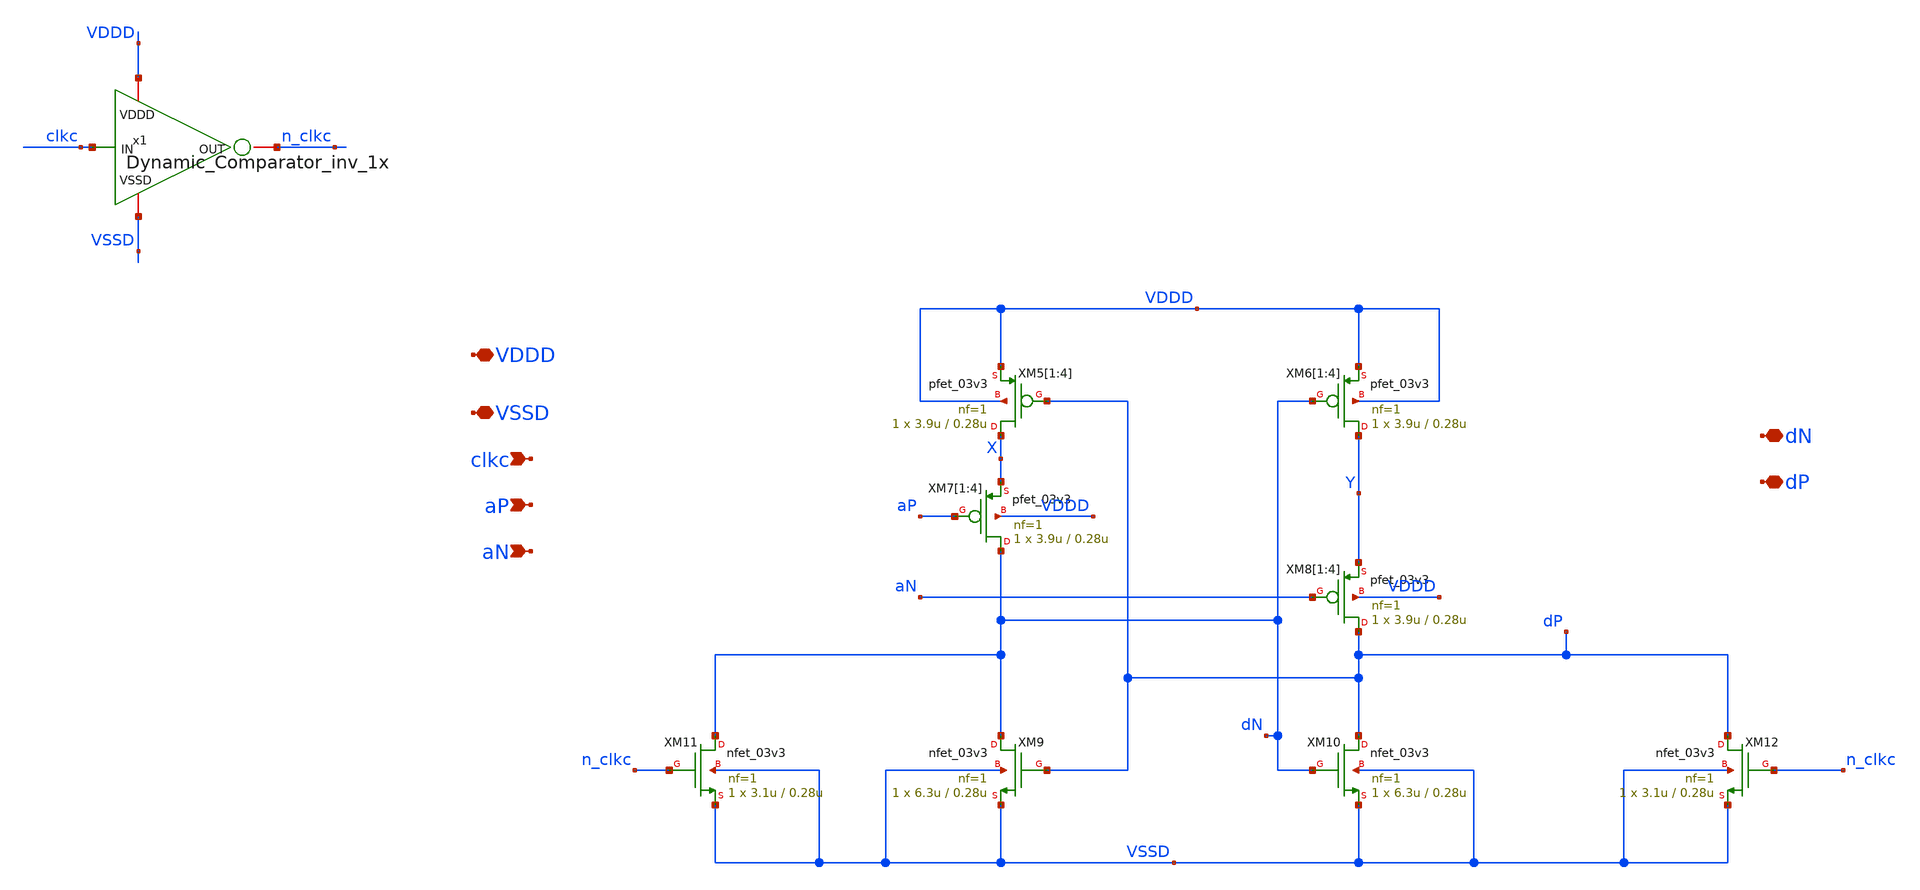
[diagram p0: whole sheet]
** sch_path: SAR_ADC/Dynamic_Comparator/xschem/Dynamic_Comparator_latch.sch
**.subckt Dynamic_Comparator_latch VDDD VSSD clkc aP aN dN dP
*.iopin VDDD
*.iopin VSSD
*.ipin clkc
*.ipin aP
*.ipin aN
*.iopin dN
*.iopin dP
XM5[1] X dP VDDD VDDD pfet_03v3 L=0.28u W=3.9u nf=1 ad='int((nf+1)/2) * W/nf * 0.18u' as='int((nf+2)/2) * W/nf * 0.18u'
+ pd='2*int((nf+1)/2) * (W/nf + 0.18u)' ps='2*int((nf+2)/2) * (W/nf + 0.18u)' nrd='0.18u / W' nrs='0.18u / W'
+ sa=0 sb=0 sd=0 m=1
XM5[2] X dP VDDD VDDD pfet_03v3 L=0.28u W=3.9u nf=1 ad='int((nf+1)/2) * W/nf * 0.18u' as='int((nf+2)/2) * W/nf * 0.18u'
+ pd='2*int((nf+1)/2) * (W/nf + 0.18u)' ps='2*int((nf+2)/2) * (W/nf + 0.18u)' nrd='0.18u / W' nrs='0.18u / W'
+ sa=0 sb=0 sd=0 m=1
XM5[3] X dP VDDD VDDD pfet_03v3 L=0.28u W=3.9u nf=1 ad='int((nf+1)/2) * W/nf * 0.18u' as='int((nf+2)/2) * W/nf * 0.18u'
+ pd='2*int((nf+1)/2) * (W/nf + 0.18u)' ps='2*int((nf+2)/2) * (W/nf + 0.18u)' nrd='0.18u / W' nrs='0.18u / W'
+ sa=0 sb=0 sd=0 m=1
XM5[4] X dP VDDD VDDD pfet_03v3 L=0.28u W=3.9u nf=1 ad='int((nf+1)/2) * W/nf * 0.18u' as='int((nf+2)/2) * W/nf * 0.18u'
+ pd='2*int((nf+1)/2) * (W/nf + 0.18u)' ps='2*int((nf+2)/2) * (W/nf + 0.18u)' nrd='0.18u / W' nrs='0.18u / W'
+ sa=0 sb=0 sd=0 m=1
XM6[1] Y dN VDDD VDDD pfet_03v3 L=0.28u W=3.9u nf=1 ad='int((nf+1)/2) * W/nf * 0.18u' as='int((nf+2)/2) * W/nf * 0.18u'
+ pd='2*int((nf+1)/2) * (W/nf + 0.18u)' ps='2*int((nf+2)/2) * (W/nf + 0.18u)' nrd='0.18u / W' nrs='0.18u / W'
+ sa=0 sb=0 sd=0 m=1
XM6[2] Y dN VDDD VDDD pfet_03v3 L=0.28u W=3.9u nf=1 ad='int((nf+1)/2) * W/nf * 0.18u' as='int((nf+2)/2) * W/nf * 0.18u'
+ pd='2*int((nf+1)/2) * (W/nf + 0.18u)' ps='2*int((nf+2)/2) * (W/nf + 0.18u)' nrd='0.18u / W' nrs='0.18u / W'
+ sa=0 sb=0 sd=0 m=1
XM6[3] Y dN VDDD VDDD pfet_03v3 L=0.28u W=3.9u nf=1 ad='int((nf+1)/2) * W/nf * 0.18u' as='int((nf+2)/2) * W/nf * 0.18u'
+ pd='2*int((nf+1)/2) * (W/nf + 0.18u)' ps='2*int((nf+2)/2) * (W/nf + 0.18u)' nrd='0.18u / W' nrs='0.18u / W'
+ sa=0 sb=0 sd=0 m=1
XM6[4] Y dN VDDD VDDD pfet_03v3 L=0.28u W=3.9u nf=1 ad='int((nf+1)/2) * W/nf * 0.18u' as='int((nf+2)/2) * W/nf * 0.18u'
+ pd='2*int((nf+1)/2) * (W/nf + 0.18u)' ps='2*int((nf+2)/2) * (W/nf + 0.18u)' nrd='0.18u / W' nrs='0.18u / W'
+ sa=0 sb=0 sd=0 m=1
XM7[1] dN aP X VDDD pfet_03v3 L=0.28u W=3.9u nf=1 ad='int((nf+1)/2) * W/nf * 0.18u' as='int((nf+2)/2) * W/nf * 0.18u'
+ pd='2*int((nf+1)/2) * (W/nf + 0.18u)' ps='2*int((nf+2)/2) * (W/nf + 0.18u)' nrd='0.18u / W' nrs='0.18u / W'
+ sa=0 sb=0 sd=0 m=1
XM7[2] dN aP X VDDD pfet_03v3 L=0.28u W=3.9u nf=1 ad='int((nf+1)/2) * W/nf * 0.18u' as='int((nf+2)/2) * W/nf * 0.18u'
+ pd='2*int((nf+1)/2) * (W/nf + 0.18u)' ps='2*int((nf+2)/2) * (W/nf + 0.18u)' nrd='0.18u / W' nrs='0.18u / W'
+ sa=0 sb=0 sd=0 m=1
XM7[3] dN aP X VDDD pfet_03v3 L=0.28u W=3.9u nf=1 ad='int((nf+1)/2) * W/nf * 0.18u' as='int((nf+2)/2) * W/nf * 0.18u'
+ pd='2*int((nf+1)/2) * (W/nf + 0.18u)' ps='2*int((nf+2)/2) * (W/nf + 0.18u)' nrd='0.18u / W' nrs='0.18u / W'
+ sa=0 sb=0 sd=0 m=1
XM7[4] dN aP X VDDD pfet_03v3 L=0.28u W=3.9u nf=1 ad='int((nf+1)/2) * W/nf * 0.18u' as='int((nf+2)/2) * W/nf * 0.18u'
+ pd='2*int((nf+1)/2) * (W/nf + 0.18u)' ps='2*int((nf+2)/2) * (W/nf + 0.18u)' nrd='0.18u / W' nrs='0.18u / W'
+ sa=0 sb=0 sd=0 m=1
XM8[1] dP aN Y VDDD pfet_03v3 L=0.28u W=3.9u nf=1 ad='int((nf+1)/2) * W/nf * 0.18u' as='int((nf+2)/2) * W/nf * 0.18u'
+ pd='2*int((nf+1)/2) * (W/nf + 0.18u)' ps='2*int((nf+2)/2) * (W/nf + 0.18u)' nrd='0.18u / W' nrs='0.18u / W'
+ sa=0 sb=0 sd=0 m=1
XM8[2] dP aN Y VDDD pfet_03v3 L=0.28u W=3.9u nf=1 ad='int((nf+1)/2) * W/nf * 0.18u' as='int((nf+2)/2) * W/nf * 0.18u'
+ pd='2*int((nf+1)/2) * (W/nf + 0.18u)' ps='2*int((nf+2)/2) * (W/nf + 0.18u)' nrd='0.18u / W' nrs='0.18u / W'
+ sa=0 sb=0 sd=0 m=1
XM8[3] dP aN Y VDDD pfet_03v3 L=0.28u W=3.9u nf=1 ad='int((nf+1)/2) * W/nf * 0.18u' as='int((nf+2)/2) * W/nf * 0.18u'
+ pd='2*int((nf+1)/2) * (W/nf + 0.18u)' ps='2*int((nf+2)/2) * (W/nf + 0.18u)' nrd='0.18u / W' nrs='0.18u / W'
+ sa=0 sb=0 sd=0 m=1
XM8[4] dP aN Y VDDD pfet_03v3 L=0.28u W=3.9u nf=1 ad='int((nf+1)/2) * W/nf * 0.18u' as='int((nf+2)/2) * W/nf * 0.18u'
+ pd='2*int((nf+1)/2) * (W/nf + 0.18u)' ps='2*int((nf+2)/2) * (W/nf + 0.18u)' nrd='0.18u / W' nrs='0.18u / W'
+ sa=0 sb=0 sd=0 m=1
XM9 dN dP VSSD VSSD nfet_03v3 L=0.28u W=6.3u nf=1 ad='int((nf+1)/2) * W/nf * 0.18u' as='int((nf+2)/2) * W/nf * 0.18u'
+ pd='2*int((nf+1)/2) * (W/nf + 0.18u)' ps='2*int((nf+2)/2) * (W/nf + 0.18u)' nrd='0.18u / W' nrs='0.18u / W'
+ sa=0 sb=0 sd=0 m=1
XM10 dP dN VSSD VSSD nfet_03v3 L=0.28u W=6.3u nf=1 ad='int((nf+1)/2) * W/nf * 0.18u' as='int((nf+2)/2) * W/nf * 0.18u'
+ pd='2*int((nf+1)/2) * (W/nf + 0.18u)' ps='2*int((nf+2)/2) * (W/nf + 0.18u)' nrd='0.18u / W' nrs='0.18u / W'
+ sa=0 sb=0 sd=0 m=1
XM11 dN n_clkc VSSD VSSD nfet_03v3 L=0.28u W=3.1u nf=1 ad='int((nf+1)/2) * W/nf * 0.18u' as='int((nf+2)/2) * W/nf * 0.18u'
+ pd='2*int((nf+1)/2) * (W/nf + 0.18u)' ps='2*int((nf+2)/2) * (W/nf + 0.18u)' nrd='0.18u / W' nrs='0.18u / W'
+ sa=0 sb=0 sd=0 m=1
XM12 dP n_clkc VSSD VSSD nfet_03v3 L=0.28u W=3.1u nf=1 ad='int((nf+1)/2) * W/nf * 0.18u' as='int((nf+2)/2) * W/nf * 0.18u'
+ pd='2*int((nf+1)/2) * (W/nf + 0.18u)' ps='2*int((nf+2)/2) * (W/nf + 0.18u)' nrd='0.18u / W' nrs='0.18u / W'
+ sa=0 sb=0 sd=0 m=1
x1 VDDD VSSD n_clkc clkc Dynamic_Comparator_inv_1x
**.ends

* expanding   symbol:  PICO_contest/Dynamic_Comparator/xschem/Dynamic_Comparator_inv_1x.sym # of
*+ pins=4
** sym_path: SAR_ADC/Dynamic_Comparator/xschem/Dynamic_Comparator_inv_1x.sym
** sch_path: SAR_ADC/Dynamic_Comparator/xschem/Dynamic_Comparator_inv_1x.sch
.subckt Dynamic_Comparator_inv_1x VDDD VSSD OUT IN
*.iopin VDDD
*.iopin VSSD
*.ipin IN
*.iopin OUT
XM1 OUT IN VSSD VSSD nfet_03v3 L=0.28u W=1.56u nf=1 ad='int((nf+1)/2) * W/nf * 0.18u' as='int((nf+2)/2) * W/nf * 0.18u'
+ pd='2*int((nf+1)/2) * (W/nf + 0.18u)' ps='2*int((nf+2)/2) * (W/nf + 0.18u)' nrd='0.18u / W' nrs='0.18u / W'
+ sa=0 sb=0 sd=0 m=1
XM2 OUT IN VDDD VDDD pfet_03v3 L=0.28u W=3.9u nf=1 ad='int((nf+1)/2) * W/nf * 0.18u' as='int((nf+2)/2) * W/nf * 0.18u'
+ pd='2*int((nf+1)/2) * (W/nf + 0.18u)' ps='2*int((nf+2)/2) * (W/nf + 0.18u)' nrd='0.18u / W' nrs='0.18u / W'
+ sa=0 sb=0 sd=0 m=1
.ends

.end
